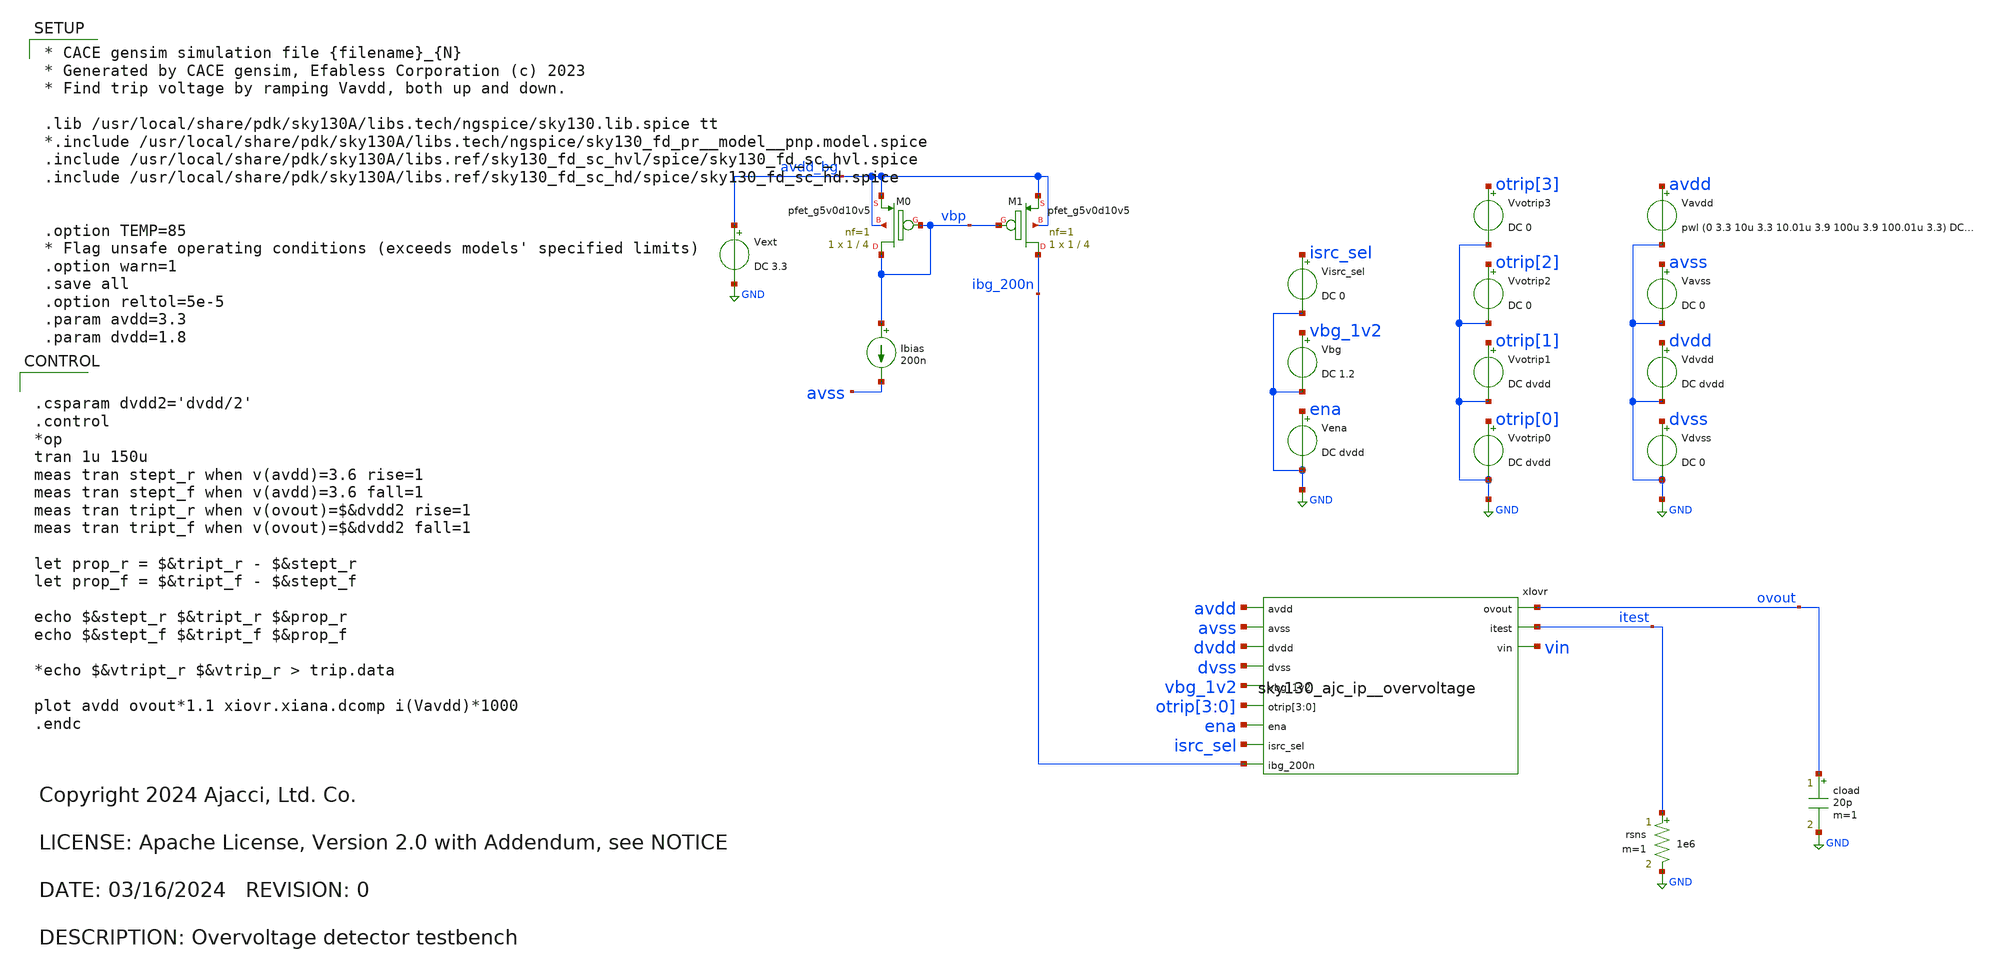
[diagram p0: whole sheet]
** sch_path: xschem/response_time.sch
* Copyright 2024 Ajacci, Ltd. Co.
* LICENSE: Apache License, Version 2.0 with Addendum, see NOTICE
**.subckt response_time
Vavss avss GND DC 0
Vena ena GND DC dvdd
Vavdd avdd GND pwl (0 3.3 10u 3.3 10.01u 3.9 100u 3.9 100.01u 3.3) DC avdd
.save i(vavdd)
Vbg vbg_1v2 GND DC 1.2
Ibias vbp avss 200n
XM1 ibg_200n vbp avdd_bg avdd_bg sky130_fd_pr__pfet_g5v0d10v5 L=4 W=1 nf=1 ad='int((nf+1)/2) * W/nf * 0.29'
+ as='int((nf+2)/2) * W/nf * 0.29' pd='2*int((nf+1)/2) * (W/nf + 0.29)' ps='2*int((nf+2)/2) * (W/nf + 0.29)'
+ nrd='0.29 / W' nrs='0.29 / W' sa=0 sb=0 sd=0 mult=1 m=1
XM0 vbp vbp avdd_bg avdd_bg sky130_fd_pr__pfet_g5v0d10v5 L=4 W=1 nf=1 ad='int((nf+1)/2) * W/nf * 0.29'
+ as='int((nf+2)/2) * W/nf * 0.29' pd='2*int((nf+1)/2) * (W/nf + 0.29)' ps='2*int((nf+2)/2) * (W/nf + 0.29)'
+ nrd='0.29 / W' nrs='0.29 / W' sa=0 sb=0 sd=0 mult=1 m=1
Vdvss dvss GND DC 0
Vdvdd dvdd GND DC dvdd
.save i(vdvdd)
rsns itest GND 1e6 m=1
cload ovout GND 20p m=1
xIovr avdd avss dvdd dvss vbg_1v2 ovout itest otrip[3] otrip[2] otrip[1] otrip[0] vin ena isrc_sel
+ ibg_200n sky130_ajc_ip__overvoltage
Vvotrip0 otrip[0] GND DC dvdd
.save i(vvotrip0)
Vvotrip1 otrip[1] GND DC dvdd
.save i(vvotrip1)
Vvotrip2 otrip[2] GND DC 0
.save i(vvotrip2)
Vvotrip3 otrip[3] GND DC 0
.save i(vvotrip3)
Visrc_sel isrc_sel GND DC 0
Vext avdd_bg GND DC 3.3
.save i(vext)
**** begin user architecture code

* CACE gensim simulation file {filename}_{N}
* Generated by CACE gensim, Efabless Corporation (c) 2023
* Find trip voltage by ramping Vavdd, both up and down.

.lib /usr/local/share/pdk/sky130A/libs.tech/ngspice/sky130.lib.spice tt
*.include /usr/local/share/pdk/sky130A/libs.tech/ngspice/sky130_fd_pr__model__pnp.model.spice
.include /usr/local/share/pdk/sky130A/libs.ref/sky130_fd_sc_hvl/spice/sky130_fd_sc_hvl.spice
.include /usr/local/share/pdk/sky130A/libs.ref/sky130_fd_sc_hd/spice/sky130_fd_sc_hd.spice


.option TEMP=85
* Flag unsafe operating conditions (exceeds models' specified limits)
.option warn=1
.save all
.option reltol=5e-5
.param avdd=3.3
.param dvdd=1.8





.csparam dvdd2='dvdd/2'
.control
*op
tran 1u 150u
meas tran stept_r when v(avdd)=3.6 rise=1
meas tran stept_f when v(avdd)=3.6 fall=1
meas tran tript_r when v(ovout)=$&dvdd2 rise=1
meas tran tript_f when v(ovout)=$&dvdd2 fall=1

let prop_r = $&tript_r - $&stept_r
let prop_f = $&tript_f - $&stept_f

echo $&stept_r $&tript_r $&prop_r
echo $&stept_f $&tript_f $&prop_f

*echo $&vtript_r $&vtrip_r > trip.data

plot avdd ovout*1.1 xiovr.xiana.dcomp i(Vavdd)*1000
.endc


**** end user architecture code
**.ends
.GLOBAL GND
.end
